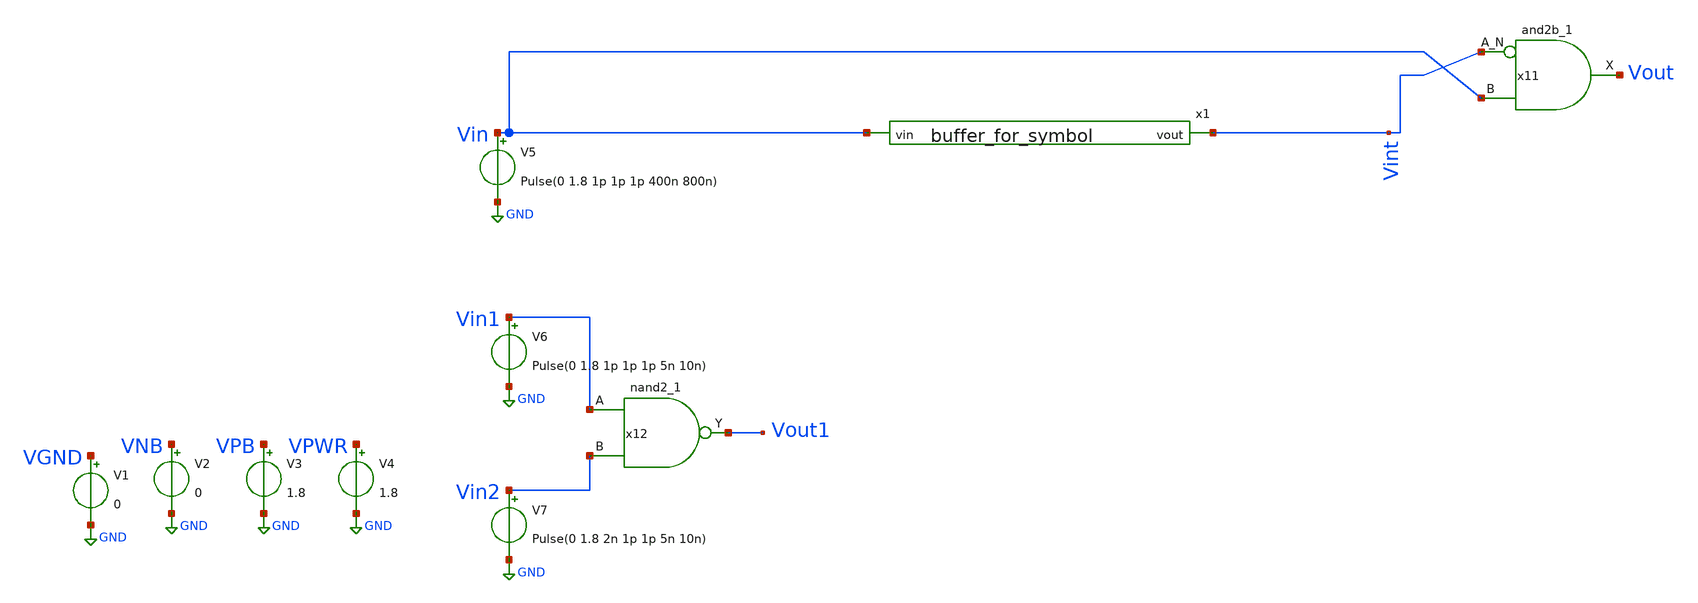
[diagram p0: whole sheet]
** sch_path: for_delay.sch
**.subckt for_delay
V1 VGND GND 0
V2 VNB GND 0
V3 VPB GND 1.8
V4 VPWR GND 1.8
V5 Vin GND Pulse(0 1.8 1p 1p 1p 400n 800n)
x11 Vint Vin VGND VNB VPB VPWR Vout sky130_fd_sc_hd__and2b_1
V6 Vin1 GND Pulse(0 1.8 1p 1p 1p 5n 10n)
V7 Vin2 GND Pulse(0 1.8 2n 1p 1p 5n 10n)
x12 Vin1 Vin2 VGND VNB VPB VPWR Vout1 sky130_fd_sc_hd__nand2_1
x1 Vin Vint buffer_for_symbol
**** begin user architecture code


.lib ~/open_pdks/sky130/sky130A/libs.tech/ngspice/sky130.lib.spice tt
.include ~/open_pdks/sky130/sky130A/libs.ref/sky130_fd_sc_hd/spice/sky130_fd_sc_hd.spice
.tran 1n 1u
.save Vin Vout Vint Vin1 Vin2 Vout1

**** end user architecture code
**.ends

* expanding   symbol:  /home/cegrahul/Desktop/fyp/buffer_for_symbol.sym # of pins=2
** sym_path: buffer_for_symbol.sym
** sch_path: buffer_for_symbol.sch
.subckt buffer_for_symbol vin vout
*.ipin vin
*.opin vout
XM1 net2 vin net1 VDD sky130_fd_pr__pfet_01v8 L=4 W=3 nf=1 ad='int((nf+1)/2) * W/nf * 0.29' as='int((nf+2)/2) * W/nf * 0.29'
+ pd='2*int((nf+1)/2) * (W/nf + 0.29)' ps='2*int((nf+2)/2) * (W/nf + 0.29)' nrd='0.29 / W' nrs='0.29 / W'
+ sa=0 sb=0 sd=0 mult=1 m=1
XM2 net2 vin net3 net3 sky130_fd_pr__nfet_01v8 L=4 W=1 nf=1 ad='int((nf+1)/2) * W/nf * 0.29' as='int((nf+2)/2) * W/nf * 0.29'
+ pd='2*int((nf+1)/2) * (W/nf + 0.29)' ps='2*int((nf+2)/2) * (W/nf + 0.29)' nrd='0.29 / W' nrs='0.29 / W'
+ sa=0 sb=0 sd=0 mult=1 m=1
V2 net1 GND 1.8
XM3 vout net2 net4 VDD sky130_fd_pr__pfet_01v8 L=4 W=3 nf=1 ad='int((nf+1)/2) * W/nf * 0.29' as='int((nf+2)/2) * W/nf * 0.29'
+ pd='2*int((nf+1)/2) * (W/nf + 0.29)' ps='2*int((nf+2)/2) * (W/nf + 0.29)' nrd='0.29 / W' nrs='0.29 / W'
+ sa=0 sb=0 sd=0 mult=1 m=1
XM4 vout net2 net5 net5 sky130_fd_pr__nfet_01v8 L=4 W=1 nf=1 ad='int((nf+1)/2) * W/nf * 0.29' as='int((nf+2)/2) * W/nf * 0.29'
+ pd='2*int((nf+1)/2) * (W/nf + 0.29)' ps='2*int((nf+2)/2) * (W/nf + 0.29)' nrd='0.29 / W' nrs='0.29 / W'
+ sa=0 sb=0 sd=0 mult=1 m=1
V3 net4 GND 1.8
V1 net3 GND -1.8
V4 net5 GND -1.8
.ends

.GLOBAL GND
.end
